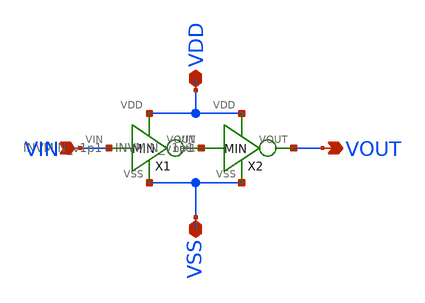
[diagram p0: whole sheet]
** sch_path: samples/cace-tests/SDC/xschem/BUFFMIN_v1p1.sch
**.subckt BUFFMIN_v1p1 VDD VSS VIN VOUT
*.iopin VDD
*.iopin VSS
*.ipin VIN
*.opin VOUT
X1 VIN net1 VDD VSS INVMIN_v1p1
X2 net1 VOUT VDD VSS INVMIN_v1p1
**.ends

* expanding   symbol:  INVMIN_v1p1.sym # of pins=4
** sym_path: samples/cace-tests/SDC/xschem/INVMIN_v1p1.sym
** sch_path: samples/cace-tests/SDC/xschem/INVMIN_v1p1.sch
.subckt INVMIN_v1p1 VIN VOUT VDD VSS
*.ipin VIN
*.iopin VDD
*.iopin VSS
*.opin VOUT
XM1 VOUT VIN VSS VSS sky130_fd_pr__nfet_01v8 L=0.15 W=1 nf=1 ad='int((nf+1)/2) * W/nf * 0.29' as='int((nf+2)/2) * W/nf * 0.29'
+ pd='2*int((nf+1)/2) * (W/nf + 0.29)' ps='2*int((nf+2)/2) * (W/nf + 0.29)' nrd='0.29 / W' nrs='0.29 / W'
+ sa=0 sb=0 sd=0 mult=1 m=1
XM2 VOUT VIN VDD VDD sky130_fd_pr__pfet_01v8 L=0.15 W=1 nf=1 ad='int((nf+1)/2) * W/nf * 0.29' as='int((nf+2)/2) * W/nf * 0.29'
+ pd='2*int((nf+1)/2) * (W/nf + 0.29)' ps='2*int((nf+2)/2) * (W/nf + 0.29)' nrd='0.29 / W' nrs='0.29 / W'
+ sa=0 sb=0 sd=0 mult=1 m=1
.ends

.end
